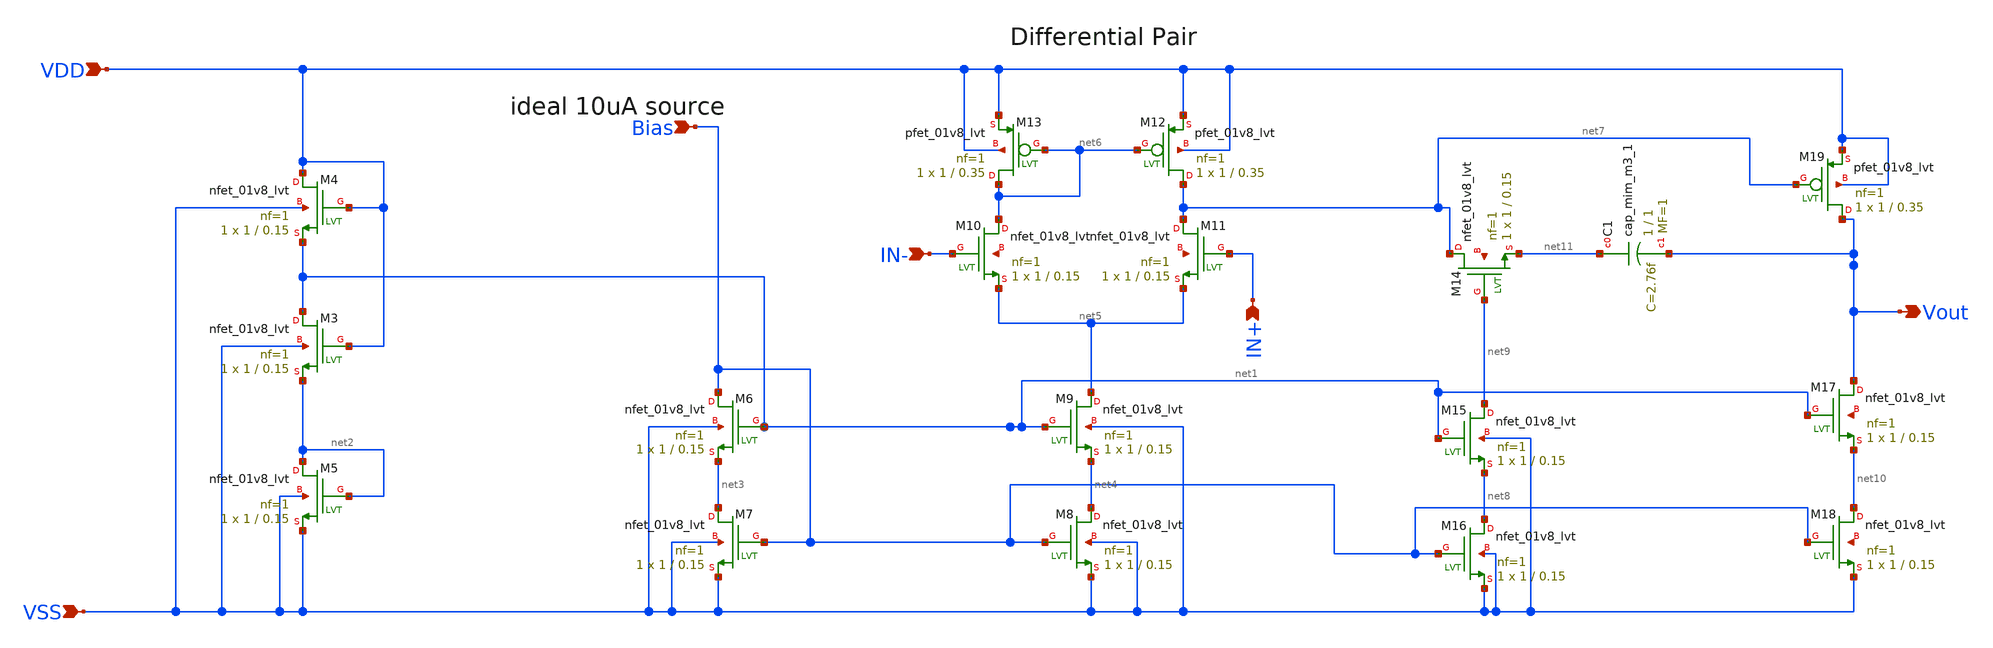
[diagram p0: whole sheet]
** sch_path: xschem_files/tinyOTA.sch
**.subckt tinyOTA Bias IN+ IN- VDD VSS Vout
*.ipin Bias
*.ipin IN+
*.ipin IN-
*.ipin VDD
*.ipin VSS
*.opin Vout
XM5 net2 net2 VSS VSS sky130_fd_pr__nfet_01v8_lvt L=0.15 W=1 nf=1 ad='int((1 + 1)/2) * 1 / 1 * 0.29'
+ as='int((1 + 2)/2) * 1 / 1 * 0.29' pd='2*int((1 + 1)/2) * (1 / 1 + 0.29)' ps='2*int((1 + 2)/2) * (1 / 1 + 0.29)'
+ nrd='0.29 / 1 ' nrs='0.29 / 1 ' sa=0 sb=0 sd=0 mult=1 m=1
XM3 net1 VDD net2 VSS sky130_fd_pr__nfet_01v8_lvt L=0.15 W=1 nf=1 ad='int((1 + 1)/2) * 1 / 1 * 0.29'
+ as='int((1 + 2)/2) * 1 / 1 * 0.29' pd='2*int((1 + 1)/2) * (1 / 1 + 0.29)' ps='2*int((1 + 2)/2) * (1 / 1 + 0.29)'
+ nrd='0.29 / 1 ' nrs='0.29 / 1 ' sa=0 sb=0 sd=0 mult=1 m=1
XM4 VDD VDD net1 VSS sky130_fd_pr__nfet_01v8_lvt L=0.15 W=1 nf=1 ad='int((1 + 1)/2) * 1 / 1 * 0.29' as='int((1 + 2)/2) * 1 / 1 * 0.29'
+ pd='2*int((1 + 1)/2) * (1 / 1 + 0.29)' ps='2*int((1 + 2)/2) * (1 / 1 + 0.29)' nrd='0.29 / 1 ' nrs='0.29 / 1 '
+ sa=0 sb=0 sd=0 mult=1 m=1
XM6 Bias net1 net3 VSS sky130_fd_pr__nfet_01v8_lvt L=0.15 W=1 nf=1 ad='int((1 + 1)/2) * 1 / 1 * 0.29'
+ as='int((1 + 2)/2) * 1 / 1 * 0.29' pd='2*int((1 + 1)/2) * (1 / 1 + 0.29)' ps='2*int((1 + 2)/2) * (1 / 1 + 0.29)'
+ nrd='0.29 / 1 ' nrs='0.29 / 1 ' sa=0 sb=0 sd=0 mult=1 m=1
XM7 net3 Bias VSS VSS sky130_fd_pr__nfet_01v8_lvt L=0.15 W=1 nf=1 ad='int((1 + 1)/2) * 1 / 1 * 0.29'
+ as='int((1 + 2)/2) * 1 / 1 * 0.29' pd='2*int((1 + 1)/2) * (1 / 1 + 0.29)' ps='2*int((1 + 2)/2) * (1 / 1 + 0.29)'
+ nrd='0.29 / 1 ' nrs='0.29 / 1 ' sa=0 sb=0 sd=0 mult=1 m=1
XM8 net4 Bias VSS VSS sky130_fd_pr__nfet_01v8_lvt L=0.15 W=1 nf=1 ad='int((1 + 1)/2) * 1 / 1 * 0.29'
+ as='int((1 + 2)/2) * 1 / 1 * 0.29' pd='2*int((1 + 1)/2) * (1 / 1 + 0.29)' ps='2*int((1 + 2)/2) * (1 / 1 + 0.29)'
+ nrd='0.29 / 1 ' nrs='0.29 / 1 ' sa=0 sb=0 sd=0 mult=1 m=1
XM9 net5 net1 net4 VSS sky130_fd_pr__nfet_01v8_lvt L=0.15 W=1 nf=1 ad='int((1 + 1)/2) * 1 / 1 * 0.29'
+ as='int((1 + 2)/2) * 1 / 1 * 0.29' pd='2*int((1 + 1)/2) * (1 / 1 + 0.29)' ps='2*int((1 + 2)/2) * (1 / 1 + 0.29)'
+ nrd='0.29 / 1 ' nrs='0.29 / 1 ' sa=0 sb=0 sd=0 mult=1 m=1
XM10 net6 IN- net5 net12 sky130_fd_pr__nfet_01v8_lvt L=0.15 W=1 nf=1 ad='int((1 + 1)/2) * 1 / 1 * 0.29'
+ as='int((1 + 2)/2) * 1 / 1 * 0.29' pd='2*int((1 + 1)/2) * (1 / 1 + 0.29)' ps='2*int((1 + 2)/2) * (1 / 1 + 0.29)'
+ nrd='0.29 / 1 ' nrs='0.29 / 1 ' sa=0 sb=0 sd=0 mult=1 m=1
XM11 net7 IN+ net5 net13 sky130_fd_pr__nfet_01v8_lvt L=0.15 W=1 nf=1 ad='int((1 + 1)/2) * 1 / 1 * 0.29'
+ as='int((1 + 2)/2) * 1 / 1 * 0.29' pd='2*int((1 + 1)/2) * (1 / 1 + 0.29)' ps='2*int((1 + 2)/2) * (1 / 1 + 0.29)'
+ nrd='0.29 / 1 ' nrs='0.29 / 1 ' sa=0 sb=0 sd=0 mult=1 m=1
XM12 net7 net6 VDD VDD sky130_fd_pr__pfet_01v8_lvt L=0.35 W=1 nf=1 ad='int((1 + 1)/2) * 1 / 1 * 0.29'
+ as='int((1 + 2)/2) * 1 / 1 * 0.29' pd='2*int((1 + 1)/2) * (1 / 1 + 0.29)' ps='2*int((1 + 2)/2) * (1 / 1 + 0.29)'
+ nrd='0.29 / 1 ' nrs='0.29 / 1 ' sa=0 sb=0 sd=0 mult=1 m=1
XM13 net6 net6 VDD VDD sky130_fd_pr__pfet_01v8_lvt L=0.35 W=1 nf=1 ad='int((1 + 1)/2) * 1 / 1 * 0.29'
+ as='int((1 + 2)/2) * 1 / 1 * 0.29' pd='2*int((1 + 1)/2) * (1 / 1 + 0.29)' ps='2*int((1 + 2)/2) * (1 / 1 + 0.29)'
+ nrd='0.29 / 1 ' nrs='0.29 / 1 ' sa=0 sb=0 sd=0 mult=1 m=1
XM14 net7 net9 net11 net14 sky130_fd_pr__nfet_01v8_lvt L=0.15 W=1 nf=1 ad='int((1 + 1)/2) * 1 / 1 * 0.29'
+ as='int((1 + 2)/2) * 1 / 1 * 0.29' pd='2*int((1 + 1)/2) * (1 / 1 + 0.29)' ps='2*int((1 + 2)/2) * (1 / 1 + 0.29)'
+ nrd='0.29 / 1 ' nrs='0.29 / 1 ' sa=0 sb=0 sd=0 mult=1 m=1
XC1 net11 Vout sky130_fd_pr__cap_mim_m3_1 W=1 L=1 MF=1 m=1
XM15 net9 net1 net8 VSS sky130_fd_pr__nfet_01v8_lvt L=0.15 W=1 nf=1 ad='int((1 + 1)/2) * 1 / 1 * 0.29'
+ as='int((1 + 2)/2) * 1 / 1 * 0.29' pd='2*int((1 + 1)/2) * (1 / 1 + 0.29)' ps='2*int((1 + 2)/2) * (1 / 1 + 0.29)'
+ nrd='0.29 / 1 ' nrs='0.29 / 1 ' sa=0 sb=0 sd=0 mult=1 m=1
XM16 net8 Bias VSS VSS sky130_fd_pr__nfet_01v8_lvt L=0.15 W=1 nf=1 ad='int((1 + 1)/2) * 1 / 1 * 0.29'
+ as='int((1 + 2)/2) * 1 / 1 * 0.29' pd='2*int((1 + 1)/2) * (1 / 1 + 0.29)' ps='2*int((1 + 2)/2) * (1 / 1 + 0.29)'
+ nrd='0.29 / 1 ' nrs='0.29 / 1 ' sa=0 sb=0 sd=0 mult=1 m=1
XM17 Vout net1 net10 net15 sky130_fd_pr__nfet_01v8_lvt L=0.15 W=1 nf=1 ad='int((1 + 1)/2) * 1 / 1 * 0.29'
+ as='int((1 + 2)/2) * 1 / 1 * 0.29' pd='2*int((1 + 1)/2) * (1 / 1 + 0.29)' ps='2*int((1 + 2)/2) * (1 / 1 + 0.29)'
+ nrd='0.29 / 1 ' nrs='0.29 / 1 ' sa=0 sb=0 sd=0 mult=1 m=1
XM18 net10 Bias VSS net16 sky130_fd_pr__nfet_01v8_lvt L=0.15 W=1 nf=1 ad='int((1 + 1)/2) * 1 / 1 * 0.29'
+ as='int((1 + 2)/2) * 1 / 1 * 0.29' pd='2*int((1 + 1)/2) * (1 / 1 + 0.29)' ps='2*int((1 + 2)/2) * (1 / 1 + 0.29)'
+ nrd='0.29 / 1 ' nrs='0.29 / 1 ' sa=0 sb=0 sd=0 mult=1 m=1
XM19 Vout net7 VDD VDD sky130_fd_pr__pfet_01v8_lvt L=0.35 W=1 nf=1 ad='int((1 + 1)/2) * 1 / 1 * 0.29'
+ as='int((1 + 2)/2) * 1 / 1 * 0.29' pd='2*int((1 + 1)/2) * (1 / 1 + 0.29)' ps='2*int((1 + 2)/2) * (1 / 1 + 0.29)'
+ nrd='0.29 / 1 ' nrs='0.29 / 1 ' sa=0 sb=0 sd=0 mult=1 m=1
**.ends
.end
